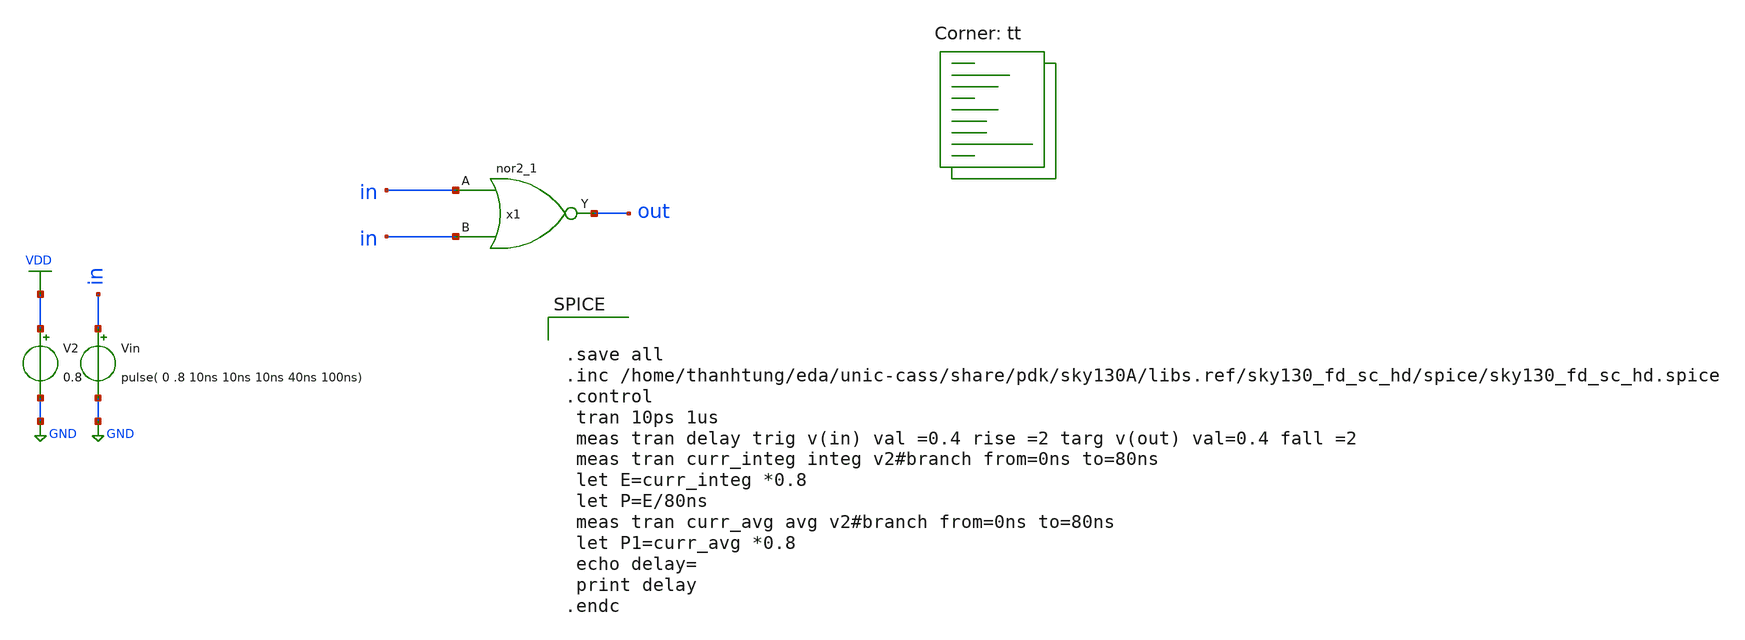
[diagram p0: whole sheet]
** sch_path: d_nor_para.sch
**.subckt d_nor_para
x1 in in GND GND VDD VDD out sky130_fd_sc_hd__nor2_1
V2 VDD GND 0.8
Vin in GND pulse( 0 .8 10ns 10ns 10ns 40ns 100ns)
**** begin user architecture code


.save all
.inc /home/thanhtung/eda/unic-cass/share/pdk/sky130A/libs.ref/sky130_fd_sc_hd/spice/sky130_fd_sc_hd.spice
.control
 tran 10ps 1us
 meas tran delay trig v(in) val =0.4 rise =2 targ v(out) val=0.4 fall =2
 meas tran curr_integ integ v2#branch from=0ns to=80ns
 let E=curr_integ *0.8
 let P=E/80ns
 meas tran curr_avg avg v2#branch from=0ns to=80ns
 let P1=curr_avg *0.8
 echo delay=
 print delay
.endc


.lib $::SKYWATER_MODELS/sky130.lib.spice tt
**** end user architecture code
**.ends
.GLOBAL GND
.GLOBAL VDD
.end
